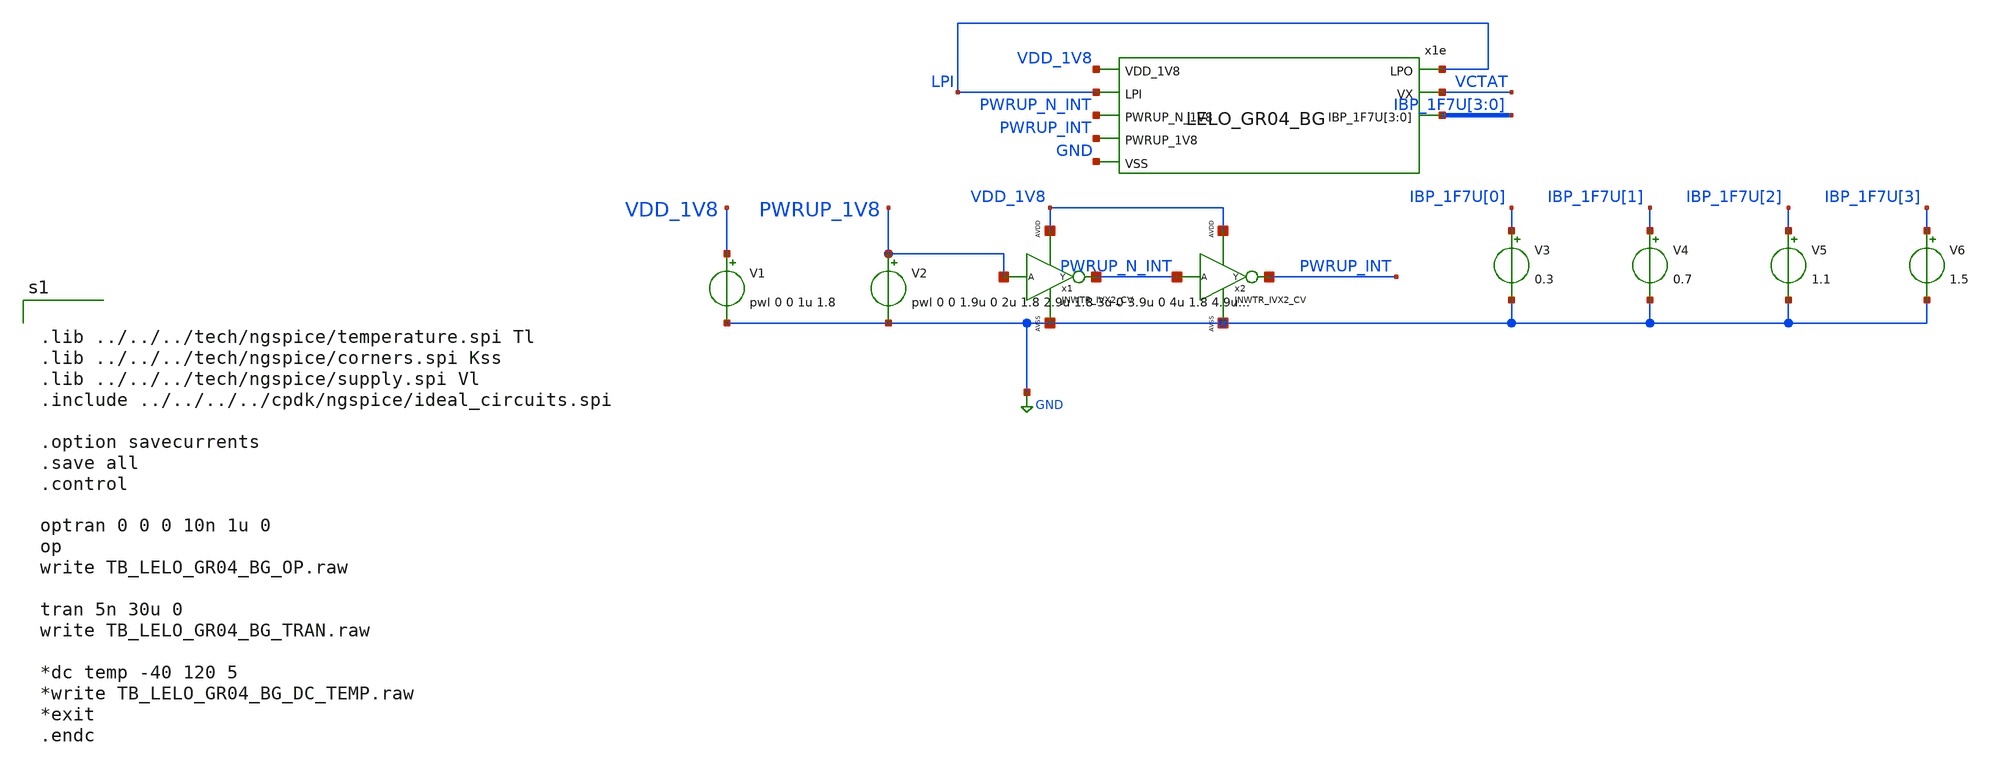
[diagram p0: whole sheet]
** sch_path: design/LELO_GR04_SKY130A/TB_LELO_GR04_BG.sch
**.subckt TB_LELO_GR04_BG
x1e VDD_1V8 LPI LPI VCTAT PWRUP_N_INT IBP_1F7U[3] IBP_1F7U[2] IBP_1F7U[1] IBP_1F7U[0] PWRUP_INT GND
+ LELO_GR04_BG
V1 VDD_1V8 GND pwl 0 0 1u 1.8
V2 PWRUP_1V8 GND pwl 0 0 1.9u 0 2u 1.8 2.9u 1.8 3u 0 3.9u 0 4u 1.8 4.9u 1.8 5u 0 7.9u 0 8u 1.8 8.9u
+ 1.8 9u 0 14.9u 0 15u 1.8 25.9u 1.8 26u 0
x1 PWRUP_1V8 PWRUP_N_INT VDD_1V8 GND JNWTR_IVX2_CV xoffset=0 yoffset=0 angle=0 M=1
x2 PWRUP_N_INT PWRUP_INT VDD_1V8 GND JNWTR_IVX2_CV xoffset=0 yoffset=0 angle=0 M=1
V3 IBP_1F7U[0] GND 0.3
V4 IBP_1F7U[1] GND 0.7
V5 IBP_1F7U[2] GND 1.1
V6 IBP_1F7U[3] GND 1.5
**** begin user architecture code


.lib ../../../tech/ngspice/temperature.spi Tl
.lib ../../../tech/ngspice/corners.spi Kss
.lib ../../../tech/ngspice/supply.spi Vl
.include ../../../../cpdk/ngspice/ideal_circuits.spi

.option savecurrents
.save all
.control

optran 0 0 0 10n 1u 0
op
write TB_LELO_GR04_BG_OP.raw

tran 5n 30u 0
write TB_LELO_GR04_BG_TRAN.raw

*dc temp -40 120 5
*write TB_LELO_GR04_BG_DC_TEMP.raw
*exit
.endc


**** end user architecture code
**.ends
.GLOBAL GND
.end
